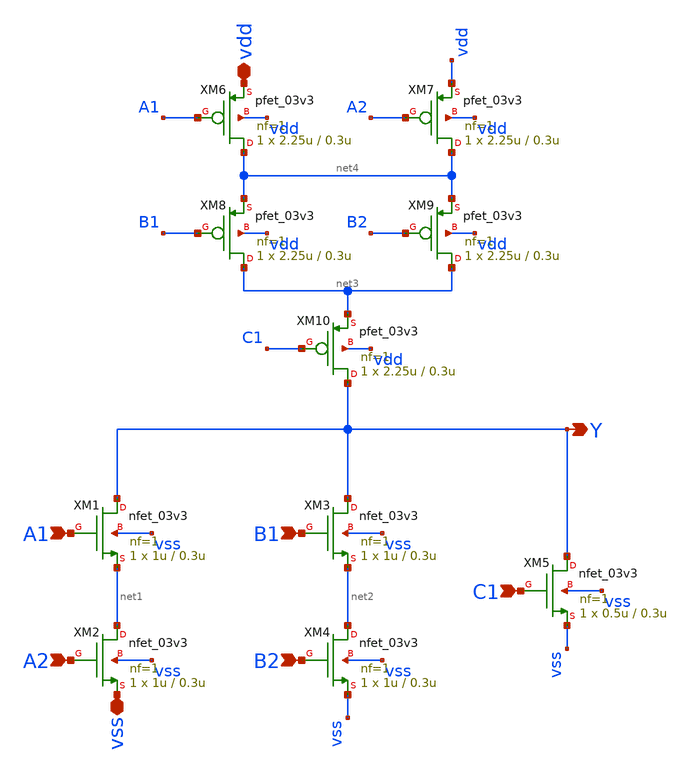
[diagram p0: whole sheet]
** sch_path: designs/aoi221/gf180mcu_gp9t3v3__aoi221_1.sch
**.subckt gf180mcu_gp9t3v3__aoi221_1 vdd vss A1 A2 B2 B1 C1 Y
*.iopin vdd
*.iopin vss
*.ipin A1
*.ipin A2
*.ipin B2
*.ipin B1
*.ipin C1
*.opin Y
XM1 Y A1 net1 vss nfet_03v3 L=0.3u W=1u nf=1 ad='int((nf+1)/2) * W/nf * 0.18u' as='int((nf+2)/2) * W/nf * 0.18u'
+ pd='2*int((nf+1)/2) * (W/nf + 0.18u)' ps='2*int((nf+2)/2) * (W/nf + 0.18u)' nrd='0.18u / W' nrs='0.18u / W'
+ sa=0 sb=0 sd=0 m=1
XM2 net1 A2 vss vss nfet_03v3 L=0.3u W=1u nf=1 ad='int((nf+1)/2) * W/nf * 0.18u' as='int((nf+2)/2) * W/nf * 0.18u'
+ pd='2*int((nf+1)/2) * (W/nf + 0.18u)' ps='2*int((nf+2)/2) * (W/nf + 0.18u)' nrd='0.18u / W' nrs='0.18u / W'
+ sa=0 sb=0 sd=0 m=1
XM3 Y B1 net2 vss nfet_03v3 L=0.3u W=1u nf=1 ad='int((nf+1)/2) * W/nf * 0.18u' as='int((nf+2)/2) * W/nf * 0.18u'
+ pd='2*int((nf+1)/2) * (W/nf + 0.18u)' ps='2*int((nf+2)/2) * (W/nf + 0.18u)' nrd='0.18u / W' nrs='0.18u / W'
+ sa=0 sb=0 sd=0 m=1
XM4 net2 B2 vss vss nfet_03v3 L=0.3u W=1u nf=1 ad='int((nf+1)/2) * W/nf * 0.18u' as='int((nf+2)/2) * W/nf * 0.18u'
+ pd='2*int((nf+1)/2) * (W/nf + 0.18u)' ps='2*int((nf+2)/2) * (W/nf + 0.18u)' nrd='0.18u / W' nrs='0.18u / W'
+ sa=0 sb=0 sd=0 m=1
XM5 Y C1 vss vss nfet_03v3 L=0.3u W=0.5u nf=1 ad='int((nf+1)/2) * W/nf * 0.18u' as='int((nf+2)/2) * W/nf * 0.18u'
+ pd='2*int((nf+1)/2) * (W/nf + 0.18u)' ps='2*int((nf+2)/2) * (W/nf + 0.18u)' nrd='0.18u / W' nrs='0.18u / W'
+ sa=0 sb=0 sd=0 m=1
XM6 net4 A1 vdd vdd pfet_03v3 L=0.3u W=2.25u nf=1 ad='int((nf+1)/2) * W/nf * 0.18u' as='int((nf+2)/2) * W/nf * 0.18u'
+ pd='2*int((nf+1)/2) * (W/nf + 0.18u)' ps='2*int((nf+2)/2) * (W/nf + 0.18u)' nrd='0.18u / W' nrs='0.18u / W'
+ sa=0 sb=0 sd=0 m=1
XM7 net4 A2 vdd vdd pfet_03v3 L=0.3u W=2.25u nf=1 ad='int((nf+1)/2) * W/nf * 0.18u' as='int((nf+2)/2) * W/nf * 0.18u'
+ pd='2*int((nf+1)/2) * (W/nf + 0.18u)' ps='2*int((nf+2)/2) * (W/nf + 0.18u)' nrd='0.18u / W' nrs='0.18u / W'
+ sa=0 sb=0 sd=0 m=1
XM8 net3 B1 net4 vdd pfet_03v3 L=0.3u W=2.25u nf=1 ad='int((nf+1)/2) * W/nf * 0.18u' as='int((nf+2)/2) * W/nf * 0.18u'
+ pd='2*int((nf+1)/2) * (W/nf + 0.18u)' ps='2*int((nf+2)/2) * (W/nf + 0.18u)' nrd='0.18u / W' nrs='0.18u / W'
+ sa=0 sb=0 sd=0 m=1
XM9 net3 B2 net4 vdd pfet_03v3 L=0.3u W=2.25u nf=1 ad='int((nf+1)/2) * W/nf * 0.18u' as='int((nf+2)/2) * W/nf * 0.18u'
+ pd='2*int((nf+1)/2) * (W/nf + 0.18u)' ps='2*int((nf+2)/2) * (W/nf + 0.18u)' nrd='0.18u / W' nrs='0.18u / W'
+ sa=0 sb=0 sd=0 m=1
XM10 Y C1 net3 vdd pfet_03v3 L=0.3u W=2.25u nf=1 ad='int((nf+1)/2) * W/nf * 0.18u' as='int((nf+2)/2) * W/nf * 0.18u'
+ pd='2*int((nf+1)/2) * (W/nf + 0.18u)' ps='2*int((nf+2)/2) * (W/nf + 0.18u)' nrd='0.18u / W' nrs='0.18u / W'
+ sa=0 sb=0 sd=0 m=1
**.ends
.end
